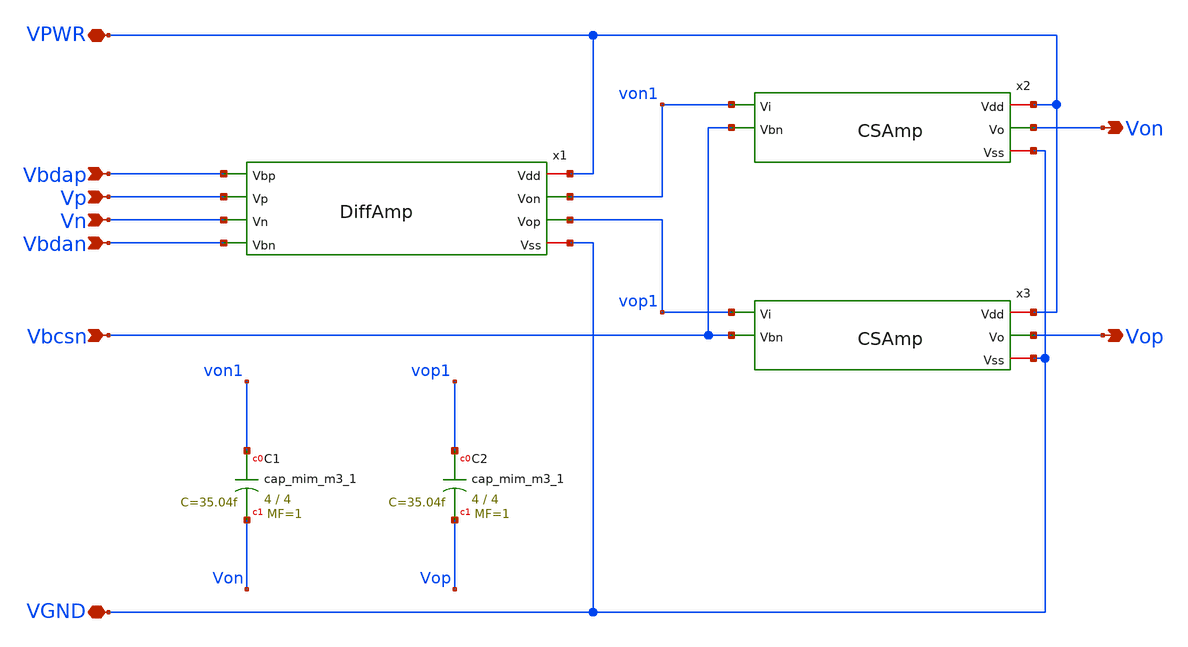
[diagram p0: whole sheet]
** sch_path: Circuits/Examples/OpAmp/MillerOpAmp.sch
**.subckt MillerOpAmp Von Vop Vbcsn Vp Vn Vbdan VPWR VGND Vbdap
*.opin Von
*.opin Vop
*.ipin Vbcsn
*.ipin Vp
*.ipin Vn
*.ipin Vbdan
*.iopin VPWR
*.iopin VGND
*.ipin Vbdap
XC1 von1 Von sky130_fd_pr__cap_mim_m3_1 W=4 L=4 MF=1 m=1
XC2 vop1 Vop sky130_fd_pr__cap_mim_m3_1 W=4 L=4 MF=1 m=1
x1 VPWR Vbdap von1 vop1 Vp Vn Vbdan VGND DiffAmp
x2 VPWR von1 Von Vbcsn VGND CSAmp
x3 VPWR vop1 Vop Vbcsn VGND CSAmp
**.ends

* expanding   symbol:  /home/jakob/Documents/RALF/Circuits/Examples/OpAmp/DiffAmp.sym # of pins=8
** sym_path: Circuits/Examples/OpAmp/DiffAmp.sym
** sch_path: Circuits/Examples/OpAmp/DiffAmp.sch
.subckt DiffAmp Vdd Vbp Von Vop Vp Vn Vbn Vss
*.iopin Vdd
*.iopin Vss
*.ipin Vp
*.ipin Vn
*.ipin Vbn
*.ipin Vbp
*.opin Vop
*.opin Von
XM1 Vop Vp vmid Vss sky130_fd_pr__nfet_01v8 L=1 W=1 nf=1 ad='int((nf+1)/2) * W/nf * 0.29' as='int((nf+2)/2) * W/nf * 0.29'
+ pd='2*int((nf+1)/2) * (W/nf + 0.29)' ps='2*int((nf+2)/2) * (W/nf + 0.29)' nrd='0.29 / W' nrs='0.29 / W'
+ sa=0 sb=0 sd=0 mult=1 m=1
XM2 Von Vn vmid Vss sky130_fd_pr__nfet_01v8 L=1 W=1 nf=1 ad='int((nf+1)/2) * W/nf * 0.29' as='int((nf+2)/2) * W/nf * 0.29'
+ pd='2*int((nf+1)/2) * (W/nf + 0.29)' ps='2*int((nf+2)/2) * (W/nf + 0.29)' nrd='0.29 / W' nrs='0.29 / W'
+ sa=0 sb=0 sd=0 mult=1 m=1
XM3 Vop Vbp Vdd Vdd sky130_fd_pr__pfet_01v8 L=1 W=2 nf=1 ad='int((nf+1)/2) * W/nf * 0.29' as='int((nf+2)/2) * W/nf * 0.29'
+ pd='2*int((nf+1)/2) * (W/nf + 0.29)' ps='2*int((nf+2)/2) * (W/nf + 0.29)' nrd='0.29 / W' nrs='0.29 / W'
+ sa=0 sb=0 sd=0 mult=1 m=1
XM4 Von Vbp Vdd Vdd sky130_fd_pr__pfet_01v8 L=1 W=2 nf=1 ad='int((nf+1)/2) * W/nf * 0.29' as='int((nf+2)/2) * W/nf * 0.29'
+ pd='2*int((nf+1)/2) * (W/nf + 0.29)' ps='2*int((nf+2)/2) * (W/nf + 0.29)' nrd='0.29 / W' nrs='0.29 / W'
+ sa=0 sb=0 sd=0 mult=1 m=1
XM5 vmid Vbn Vss Vss sky130_fd_pr__nfet_01v8 L=2 W=1 nf=1 ad='int((nf+1)/2) * W/nf * 0.29' as='int((nf+2)/2) * W/nf * 0.29'
+ pd='2*int((nf+1)/2) * (W/nf + 0.29)' ps='2*int((nf+2)/2) * (W/nf + 0.29)' nrd='0.29 / W' nrs='0.29 / W'
+ sa=0 sb=0 sd=0 mult=1 m=1
.ends


* expanding   symbol:  /home/jakob/Documents/RALF/Circuits/Examples/OpAmp/CSAmp.sym # of pins=5
** sym_path: Circuits/Examples/OpAmp/CSAmp.sym
** sch_path: Circuits/Examples/OpAmp/CSAmp.sch
.subckt CSAmp Vdd Vi Vo Vbn Vss
*.ipin Vbn
*.ipin Vi
*.iopin Vdd
*.iopin Vss
*.opin Vo
XM1 Vo Vi Vdd Vdd sky130_fd_pr__pfet_01v8 L=1 W=8 nf=1 ad='int((nf+1)/2) * W/nf * 0.29' as='int((nf+2)/2) * W/nf * 0.29'
+ pd='2*int((nf+1)/2) * (W/nf + 0.29)' ps='2*int((nf+2)/2) * (W/nf + 0.29)' nrd='0.29 / W' nrs='0.29 / W'
+ sa=0 sb=0 sd=0 mult=1 m=1
XM2 Vo Vbn Vss Vss sky130_fd_pr__nfet_01v8 L=2 W=10 nf=1 ad='int((nf+1)/2) * W/nf * 0.29' as='int((nf+2)/2) * W/nf * 0.29'
+ pd='2*int((nf+1)/2) * (W/nf + 0.29)' ps='2*int((nf+2)/2) * (W/nf + 0.29)' nrd='0.29 / W' nrs='0.29 / W'
+ sa=0 sb=0 sd=0 mult=1 m=1
XM3 Vo Vi Vdd Vdd sky130_fd_pr__pfet_01v8 L=1 W=8 nf=1 ad='int((nf+1)/2) * W/nf * 0.29' as='int((nf+2)/2) * W/nf * 0.29'
+ pd='2*int((nf+1)/2) * (W/nf + 0.29)' ps='2*int((nf+2)/2) * (W/nf + 0.29)' nrd='0.29 / W' nrs='0.29 / W'
+ sa=0 sb=0 sd=0 mult=1 m=1
XM4 Vo Vbn Vss Vss sky130_fd_pr__nfet_01v8 L=2 W=10 nf=1 ad='int((nf+1)/2) * W/nf * 0.29' as='int((nf+2)/2) * W/nf * 0.29'
+ pd='2*int((nf+1)/2) * (W/nf + 0.29)' ps='2*int((nf+2)/2) * (W/nf + 0.29)' nrd='0.29 / W' nrs='0.29 / W'
+ sa=0 sb=0 sd=0 mult=1 m=1
.ends

.end
